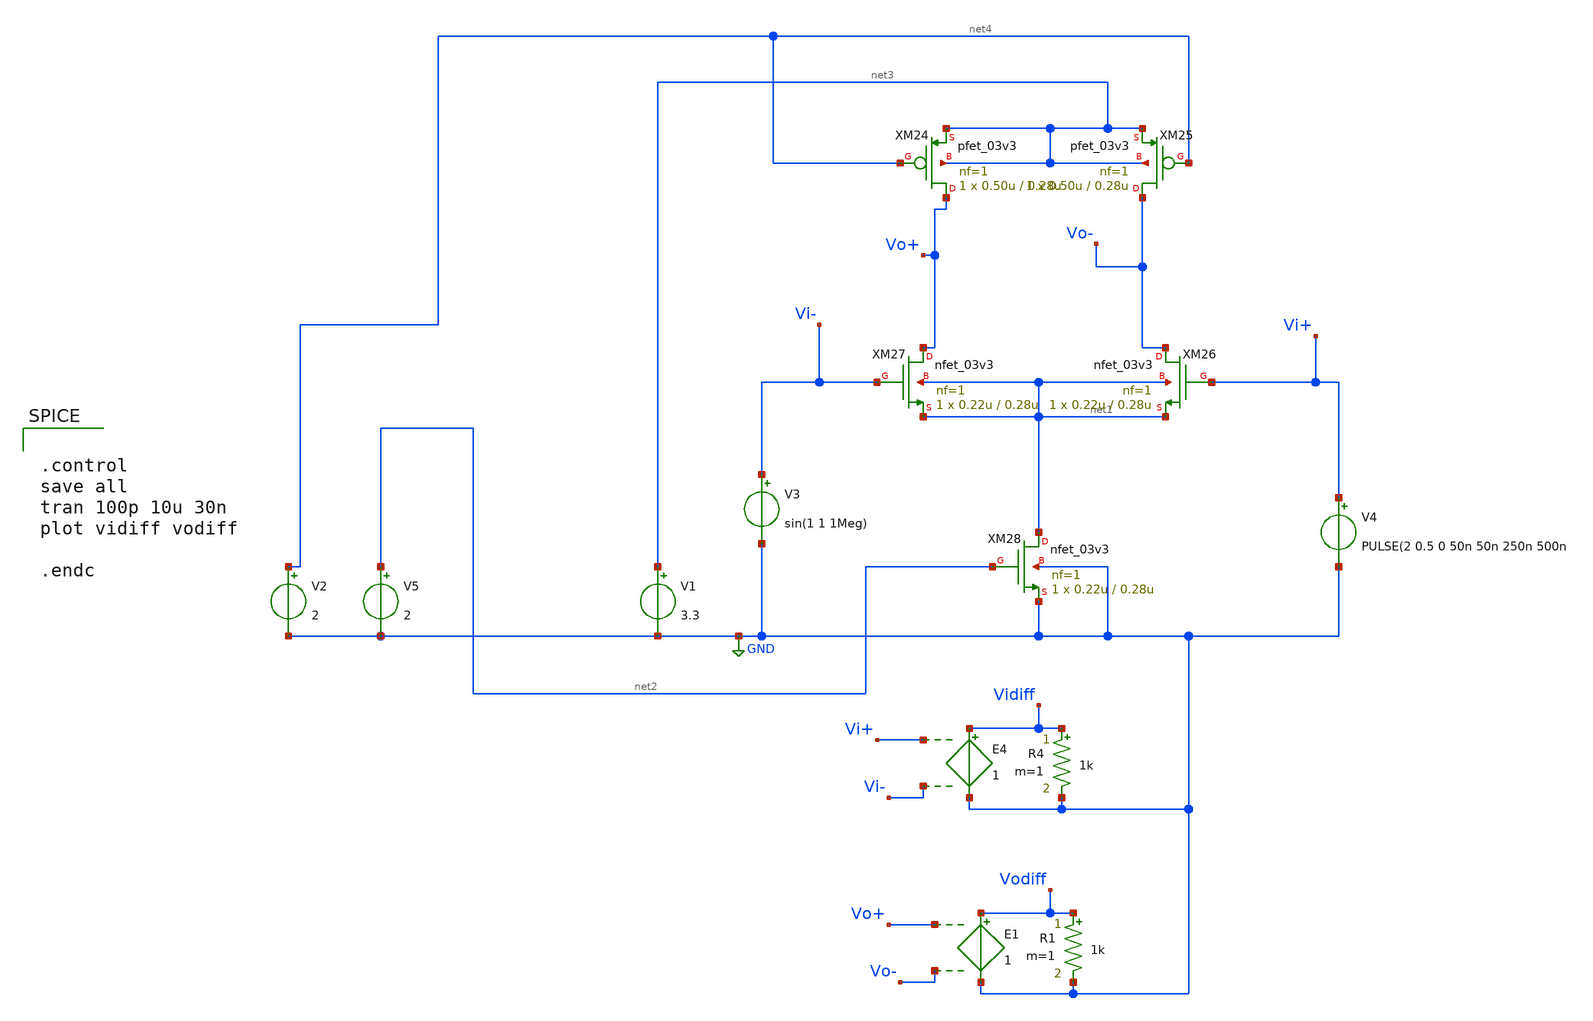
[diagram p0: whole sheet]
** sch_path: preamp/strongarm_preamp_nclk.sch
**.subckt strongarm_preamp_nclk
XM26 Vo- Vi+ net1 net1 nfet_03v3 L=0.28u W=0.22u nf=1 ad='int((nf+1)/2) * W/nf * 0.18u' as='int((nf+2)/2) * W/nf * 0.18u'
+ pd='2*int((nf+1)/2) * (W/nf + 0.18u)' ps='2*int((nf+2)/2) * (W/nf + 0.18u)' nrd='0.18u / W' nrs='0.18u / W'
+ sa=0 sb=0 sd=0 m=1
XM27 Vo+ Vi- net1 net1 nfet_03v3 L=0.28u W=0.22u nf=1 ad='int((nf+1)/2) * W/nf * 0.18u' as='int((nf+2)/2) * W/nf * 0.18u'
+ pd='2*int((nf+1)/2) * (W/nf + 0.18u)' ps='2*int((nf+2)/2) * (W/nf + 0.18u)' nrd='0.18u / W' nrs='0.18u / W'
+ sa=0 sb=0 sd=0 m=1
V3 Vi- GND sin(1 1 1Meg)
V4 Vi+ GND PULSE(2 0.5 0 50n 50n 250n 500n
R4 Vidiff GND 1k m=1
E4 Vidiff GND Vi+ Vi- 1
XM28 net1 net2 GND GND nfet_03v3 L=0.28u W=0.22u nf=1 ad='int((nf+1)/2) * W/nf * 0.18u' as='int((nf+2)/2) * W/nf * 0.18u'
+ pd='2*int((nf+1)/2) * (W/nf + 0.18u)' ps='2*int((nf+2)/2) * (W/nf + 0.18u)' nrd='0.18u / W' nrs='0.18u / W'
+ sa=0 sb=0 sd=0 m=1
V5 net2 GND 2
XM24 Vo+ net4 net3 net3 pfet_03v3 L=0.28u W=0.50u nf=1 ad='int((nf+1)/2) * W/nf * 0.18u' as='int((nf+2)/2) * W/nf * 0.18u'
+ pd='2*int((nf+1)/2) * (W/nf + 0.18u)' ps='2*int((nf+2)/2) * (W/nf + 0.18u)' nrd='0.18u / W' nrs='0.18u / W'
+ sa=0 sb=0 sd=0 m=1
XM25 Vo- net4 net3 net3 pfet_03v3 L=0.28u W=0.50u nf=1 ad='int((nf+1)/2) * W/nf * 0.18u' as='int((nf+2)/2) * W/nf * 0.18u'
+ pd='2*int((nf+1)/2) * (W/nf + 0.18u)' ps='2*int((nf+2)/2) * (W/nf + 0.18u)' nrd='0.18u / W' nrs='0.18u / W'
+ sa=0 sb=0 sd=0 m=1
R1 Vodiff GND 1k m=1
E1 Vodiff GND Vo+ Vo- 1
V1 net3 GND 3.3
V2 net4 GND 2
**** begin user architecture code

.include /foss/pdks/gf180mcuC/libs.tech/ngspice/design.ngspice
.lib /foss/pdks/gf180mcuC/libs.tech/ngspice/sm141064.ngspice typical



.control
save all
tran 100p 10u 30n
plot vidiff vodiff

.endc

**** end user architecture code
**.ends
.GLOBAL GND
.end
